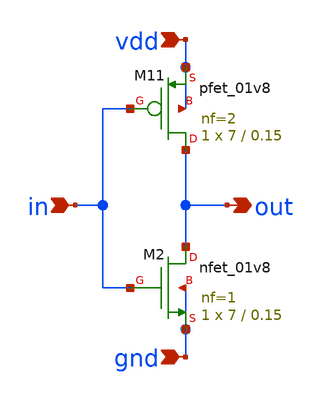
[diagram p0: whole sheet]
** sch_path: pll/Integeration/circuit_integeration/tests/test_div/divider_design/inv/xschem/inv.sch
**.subckt inv vdd in gnd out
*.ipin vdd
*.ipin in
*.ipin gnd
*.opin out
XM11 out in vdd vdd sky130_fd_pr__pfet_01v8 L=0.15 W=7 nf=2 ad='int((nf+1)/2) * W/nf * 0.29' as='int((nf+2)/2) * W/nf * 0.29'
+ pd='2*int((nf+1)/2) * (W/nf + 0.29)' ps='2*int((nf+2)/2) * (W/nf + 0.29)' nrd='0.29 / W' nrs='0.29 / W'
+ sa=0 sb=0 sd=0 mult=1 m=1
XM2 out in gnd gnd sky130_fd_pr__nfet_01v8 L=0.15 W=7 nf=1 ad='int((1 + 1)/2) * 7 / 1 * 0.29' as='int((1 + 2)/2) * 7 / 1 * 0.29'
+ pd='2*int((1 + 1)/2) * (7 / 1 + 0.29)' ps='2*int((1 + 2)/2) * (7 / 1 + 0.29)' nrd='0.29 / 7 ' nrs='0.29 / 7 '
+ sa=0 sb=0 sd=0 mult=1 m=1
**.ends
.end
